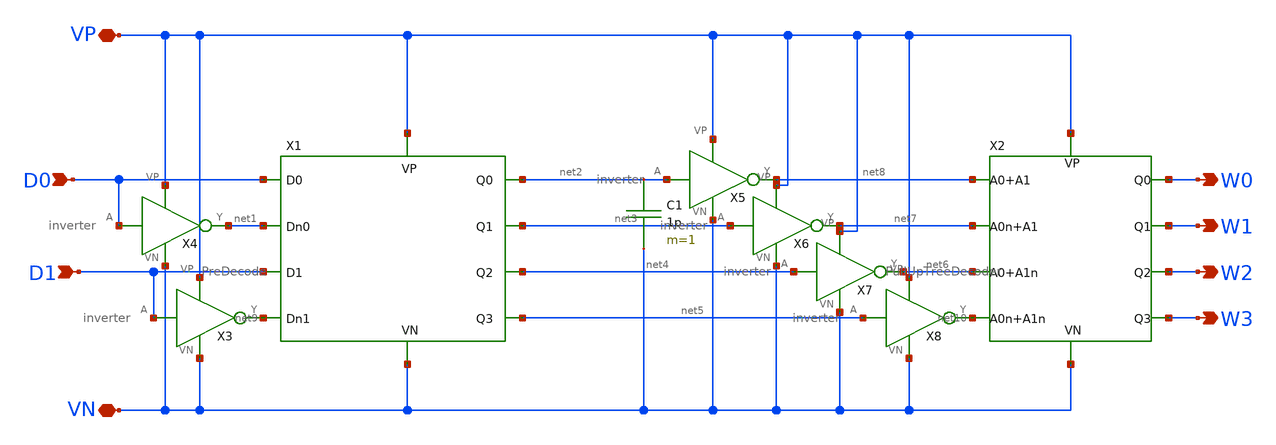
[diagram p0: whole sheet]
** sch_path: DRAM_Components/Schematic/Decoder.sch
**.subckt Decoder D1 D0 VP VN W0 W1 W2 W3
*.ipin D1
*.ipin D0
*.iopin VP
*.iopin VN
*.opin W0
*.opin W1
*.opin W2
*.opin W3
X1 net2 VP VN net3 net4 net5 net9 D1 net1 D0 PreDecode
X3 D1 net9 VP VN inverter
X4 D0 net1 VP VN inverter
X2 W0 VP VN W1 W2 W3 net10 net6 net7 net8 PullUpTreeDecoder
X5 net2 net8 VP VN inverter
X7 net4 net6 VP VN inverter
X8 net5 net10 VP VN inverter
C1 net2 VN 1p m=1
X6 net3 net7 VP VN inverter
**.ends

* expanding   symbol:  /home/madvlsi/Desktop/CMOSDRAM/DRAM_Components/Schematic/PreDecode.sym # of
*+ pins=10
** sym_path: DRAM_Components/Schematic/PreDecode.sym
** sch_path: DRAM_Components/Schematic/PreDecode.sch
.subckt PreDecode Q0 VP VN Q1 Q2 Q3 A1n A1 A0n A0
*.ipin A0
*.ipin A0n
*.ipin A1
*.ipin A1n
*.opin Q0
*.opin Q1
*.opin Q2
*.opin Q3
*.iopin VP
*.iopin VN
XM2 VP A1n net2 VP sky130_fd_pr__pfet_01v8 L=0.15 W=4 nf=1 ad='int((nf+1)/2) * W/nf * 0.29' as='int((nf+2)/2) * W/nf * 0.29'
+ pd='2*int((nf+1)/2) * (W/nf + 0.29)' ps='2*int((nf+2)/2) * (W/nf + 0.29)' nrd='0.29 / W' nrs='0.29 / W'
+ sa=0 sb=0 sd=0 mult=1 m=1
XM1 VP A1 net1 VP sky130_fd_pr__pfet_01v8 L=0.15 W=4 nf=1 ad='int((nf+1)/2) * W/nf * 0.29' as='int((nf+2)/2) * W/nf * 0.29'
+ pd='2*int((nf+1)/2) * (W/nf + 0.29)' ps='2*int((nf+2)/2) * (W/nf + 0.29)' nrd='0.29 / W' nrs='0.29 / W'
+ sa=0 sb=0 sd=0 mult=1 m=1
XM5 Q0 A0 VN VN sky130_fd_pr__nfet_01v8 L=0.15 W=1 nf=1 ad='int((nf+1)/2) * W/nf * 0.29' as='int((nf+2)/2) * W/nf * 0.29'
+ pd='2*int((nf+1)/2) * (W/nf + 0.29)' ps='2*int((nf+2)/2) * (W/nf + 0.29)' nrd='0.29 / W' nrs='0.29 / W'
+ sa=0 sb=0 sd=0 mult=1 m=1
XM3 Q1 A0n net1 VP sky130_fd_pr__pfet_01v8 L=0.15 W=2 nf=1 ad='int((nf+1)/2) * W/nf * 0.29' as='int((nf+2)/2) * W/nf * 0.29'
+ pd='2*int((nf+1)/2) * (W/nf + 0.29)' ps='2*int((nf+2)/2) * (W/nf + 0.29)' nrd='0.29 / W' nrs='0.29 / W'
+ sa=0 sb=0 sd=0 mult=1 m=1
XM4 Q0 A0 net1 VP sky130_fd_pr__pfet_01v8 L=0.15 W=2 nf=1 ad='int((nf+1)/2) * W/nf * 0.29' as='int((nf+2)/2) * W/nf * 0.29'
+ pd='2*int((nf+1)/2) * (W/nf + 0.29)' ps='2*int((nf+2)/2) * (W/nf + 0.29)' nrd='0.29 / W' nrs='0.29 / W'
+ sa=0 sb=0 sd=0 mult=1 m=1
XM6 Q0 A0 VN VN sky130_fd_pr__nfet_01v8 L=0.15 W=1 nf=1 ad='int((nf+1)/2) * W/nf * 0.29' as='int((nf+2)/2) * W/nf * 0.29'
+ pd='2*int((nf+1)/2) * (W/nf + 0.29)' ps='2*int((nf+2)/2) * (W/nf + 0.29)' nrd='0.29 / W' nrs='0.29 / W'
+ sa=0 sb=0 sd=0 mult=1 m=1
XM7 Q1 A0n VN VN sky130_fd_pr__nfet_01v8 L=0.15 W=1 nf=1 ad='int((nf+1)/2) * W/nf * 0.29' as='int((nf+2)/2) * W/nf * 0.29'
+ pd='2*int((nf+1)/2) * (W/nf + 0.29)' ps='2*int((nf+2)/2) * (W/nf + 0.29)' nrd='0.29 / W' nrs='0.29 / W'
+ sa=0 sb=0 sd=0 mult=1 m=1
XM8 Q1 A0n VN VN sky130_fd_pr__nfet_01v8 L=0.15 W=1 nf=1 ad='int((nf+1)/2) * W/nf * 0.29' as='int((nf+2)/2) * W/nf * 0.29'
+ pd='2*int((nf+1)/2) * (W/nf + 0.29)' ps='2*int((nf+2)/2) * (W/nf + 0.29)' nrd='0.29 / W' nrs='0.29 / W'
+ sa=0 sb=0 sd=0 mult=1 m=1
XM9 Q2 A1 VN VN sky130_fd_pr__nfet_01v8 L=0.15 W=1 nf=1 ad='int((nf+1)/2) * W/nf * 0.29' as='int((nf+2)/2) * W/nf * 0.29'
+ pd='2*int((nf+1)/2) * (W/nf + 0.29)' ps='2*int((nf+2)/2) * (W/nf + 0.29)' nrd='0.29 / W' nrs='0.29 / W'
+ sa=0 sb=0 sd=0 mult=1 m=1
XM10 Q2 A1 VN VN sky130_fd_pr__nfet_01v8 L=0.15 W=1 nf=1 ad='int((nf+1)/2) * W/nf * 0.29' as='int((nf+2)/2) * W/nf * 0.29'
+ pd='2*int((nf+1)/2) * (W/nf + 0.29)' ps='2*int((nf+2)/2) * (W/nf + 0.29)' nrd='0.29 / W' nrs='0.29 / W'
+ sa=0 sb=0 sd=0 mult=1 m=1
XM11 Q3 A1n VN VN sky130_fd_pr__nfet_01v8 L=0.15 W=1 nf=1 ad='int((nf+1)/2) * W/nf * 0.29' as='int((nf+2)/2) * W/nf * 0.29'
+ pd='2*int((nf+1)/2) * (W/nf + 0.29)' ps='2*int((nf+2)/2) * (W/nf + 0.29)' nrd='0.29 / W' nrs='0.29 / W'
+ sa=0 sb=0 sd=0 mult=1 m=1
XM12 Q3 A1n VN VN sky130_fd_pr__nfet_01v8 L=0.15 W=1 nf=1 ad='int((nf+1)/2) * W/nf * 0.29' as='int((nf+2)/2) * W/nf * 0.29'
+ pd='2*int((nf+1)/2) * (W/nf + 0.29)' ps='2*int((nf+2)/2) * (W/nf + 0.29)' nrd='0.29 / W' nrs='0.29 / W'
+ sa=0 sb=0 sd=0 mult=1 m=1
XM13 Q3 A1n net2 VP sky130_fd_pr__pfet_01v8 L=0.15 W=2 nf=1 ad='int((nf+1)/2) * W/nf * 0.29' as='int((nf+2)/2) * W/nf * 0.29'
+ pd='2*int((nf+1)/2) * (W/nf + 0.29)' ps='2*int((nf+2)/2) * (W/nf + 0.29)' nrd='0.29 / W' nrs='0.29 / W'
+ sa=0 sb=0 sd=0 mult=1 m=1
XM14 Q2 A1 net2 VP sky130_fd_pr__pfet_01v8 L=0.15 W=2 nf=1 ad='int((nf+1)/2) * W/nf * 0.29' as='int((nf+2)/2) * W/nf * 0.29'
+ pd='2*int((nf+1)/2) * (W/nf + 0.29)' ps='2*int((nf+2)/2) * (W/nf + 0.29)' nrd='0.29 / W' nrs='0.29 / W'
+ sa=0 sb=0 sd=0 mult=1 m=1
.ends


* expanding   symbol:  /home/madvlsi/Desktop/CMOSDRAM/DRAM_Components/Schematic/inverter.sym # of
*+ pins=4
** sym_path: DRAM_Components/Schematic/inverter.sym
** sch_path: DRAM_Components/Schematic/inverter.sch
.subckt inverter A Y VP VN
*.ipin A
*.iopin VP
*.opin Y
*.iopin VN
XM1 Y A VP VP sky130_fd_pr__pfet_01v8 L=0.15 W=1 nf=1 ad='int((nf+1)/2) * W/nf * 0.29' as='int((nf+2)/2) * W/nf * 0.29'
+ pd='2*int((nf+1)/2) * (W/nf + 0.29)' ps='2*int((nf+2)/2) * (W/nf + 0.29)' nrd='0.29 / W' nrs='0.29 / W'
+ sa=0 sb=0 sd=0 mult=1 m=1
XM2 Y A VN VN sky130_fd_pr__nfet_01v8 L=0.15 W=1 nf=1 ad='int((nf+1)/2) * W/nf * 0.29' as='int((nf+2)/2) * W/nf * 0.29'
+ pd='2*int((nf+1)/2) * (W/nf + 0.29)' ps='2*int((nf+2)/2) * (W/nf + 0.29)' nrd='0.29 / W' nrs='0.29 / W'
+ sa=0 sb=0 sd=0 mult=1 m=1
.ends


* expanding   symbol:
*+  /home/madvlsi/Desktop/CMOSDRAM/DRAM_Components/Schematic/PullUpTreeDecoder.sym # of pins=10
** sym_path: DRAM_Components/Schematic/PullUpTreeDecoder.sym
** sch_path: DRAM_Components/Schematic/PullUpTreeDecoder.sch
.subckt PullUpTreeDecoder Q0 VP VN Q1 Q2 Q3 A0nA1n A0A1n A0nA1 A0A1
*.iopin VP
*.iopin VN
*.ipin A0A1
*.ipin A0nA1
*.ipin A0A1n
*.ipin A0nA1n
*.opin Q0
*.opin Q1
*.opin Q2
*.opin Q3
XM2 Q0 A0A1 VN VN sky130_fd_pr__nfet_01v8 L=0.15 W=2 nf=1 ad='int((nf+1)/2) * W/nf * 0.29' as='int((nf+2)/2) * W/nf * 0.29'
+ pd='2*int((nf+1)/2) * (W/nf + 0.29)' ps='2*int((nf+2)/2) * (W/nf + 0.29)' nrd='0.29 / W' nrs='0.29 / W'
+ sa=0 sb=0 sd=0 mult=1 m=1
XM3 Q1 A0nA1 VP VP sky130_fd_pr__pfet_01v8 L=0.15 W=4 nf=1 ad='int((nf+1)/2) * W/nf * 0.29' as='int((nf+2)/2) * W/nf * 0.29'
+ pd='2*int((nf+1)/2) * (W/nf + 0.29)' ps='2*int((nf+2)/2) * (W/nf + 0.29)' nrd='0.29 / W' nrs='0.29 / W'
+ sa=0 sb=0 sd=0 mult=1 m=1
XM4 Q0 A0A1 VP VP sky130_fd_pr__pfet_01v8 L=0.15 W=4 nf=1 ad='int((nf+1)/2) * W/nf * 0.29' as='int((nf+2)/2) * W/nf * 0.29'
+ pd='2*int((nf+1)/2) * (W/nf + 0.29)' ps='2*int((nf+2)/2) * (W/nf + 0.29)' nrd='0.29 / W' nrs='0.29 / W'
+ sa=0 sb=0 sd=0 mult=1 m=1
XM5 Q2 A0A1n VP VP sky130_fd_pr__pfet_01v8 L=0.15 W=4 nf=1 ad='int((nf+1)/2) * W/nf * 0.29' as='int((nf+2)/2) * W/nf * 0.29'
+ pd='2*int((nf+1)/2) * (W/nf + 0.29)' ps='2*int((nf+2)/2) * (W/nf + 0.29)' nrd='0.29 / W' nrs='0.29 / W'
+ sa=0 sb=0 sd=0 mult=1 m=1
XM6 Q3 A0nA1n VP VP sky130_fd_pr__pfet_01v8 L=0.15 W=4 nf=1 ad='int((nf+1)/2) * W/nf * 0.29' as='int((nf+2)/2) * W/nf * 0.29'
+ pd='2*int((nf+1)/2) * (W/nf + 0.29)' ps='2*int((nf+2)/2) * (W/nf + 0.29)' nrd='0.29 / W' nrs='0.29 / W'
+ sa=0 sb=0 sd=0 mult=1 m=1
XM7 Q1 A0nA1 VN VN sky130_fd_pr__nfet_01v8 L=0.15 W=2 nf=1 ad='int((nf+1)/2) * W/nf * 0.29' as='int((nf+2)/2) * W/nf * 0.29'
+ pd='2*int((nf+1)/2) * (W/nf + 0.29)' ps='2*int((nf+2)/2) * (W/nf + 0.29)' nrd='0.29 / W' nrs='0.29 / W'
+ sa=0 sb=0 sd=0 mult=1 m=1
XM8 Q2 A0A1n VN VN sky130_fd_pr__nfet_01v8 L=0.15 W=2 nf=1 ad='int((nf+1)/2) * W/nf * 0.29' as='int((nf+2)/2) * W/nf * 0.29'
+ pd='2*int((nf+1)/2) * (W/nf + 0.29)' ps='2*int((nf+2)/2) * (W/nf + 0.29)' nrd='0.29 / W' nrs='0.29 / W'
+ sa=0 sb=0 sd=0 mult=1 m=1
XM9 Q3 A0nA1n VN VN sky130_fd_pr__nfet_01v8 L=0.15 W=2 nf=1 ad='int((nf+1)/2) * W/nf * 0.29' as='int((nf+2)/2) * W/nf * 0.29'
+ pd='2*int((nf+1)/2) * (W/nf + 0.29)' ps='2*int((nf+2)/2) * (W/nf + 0.29)' nrd='0.29 / W' nrs='0.29 / W'
+ sa=0 sb=0 sd=0 mult=1 m=1
XM1 VP VP Q0 VP sky130_fd_pr__pfet_01v8 L=0.15 W=4 nf=1 ad='int((nf+1)/2) * W/nf * 0.29' as='int((nf+2)/2) * W/nf * 0.29'
+ pd='2*int((nf+1)/2) * (W/nf + 0.29)' ps='2*int((nf+2)/2) * (W/nf + 0.29)' nrd='0.29 / W' nrs='0.29 / W'
+ sa=0 sb=0 sd=0 mult=1 m=1
XM10 VN VN Q0 VN sky130_fd_pr__nfet_01v8 L=0.15 W=2 nf=1 ad='int((nf+1)/2) * W/nf * 0.29' as='int((nf+2)/2) * W/nf * 0.29'
+ pd='2*int((nf+1)/2) * (W/nf + 0.29)' ps='2*int((nf+2)/2) * (W/nf + 0.29)' nrd='0.29 / W' nrs='0.29 / W'
+ sa=0 sb=0 sd=0 mult=1 m=1
XM11 VN VN Q3 VN sky130_fd_pr__nfet_01v8 L=0.15 W=2 nf=1 ad='int((nf+1)/2) * W/nf * 0.29' as='int((nf+2)/2) * W/nf * 0.29'
+ pd='2*int((nf+1)/2) * (W/nf + 0.29)' ps='2*int((nf+2)/2) * (W/nf + 0.29)' nrd='0.29 / W' nrs='0.29 / W'
+ sa=0 sb=0 sd=0 mult=1 m=1
XM12 VN VN Q1 VN sky130_fd_pr__nfet_01v8 L=0.15 W=2 nf=1 ad='int((nf+1)/2) * W/nf * 0.29' as='int((nf+2)/2) * W/nf * 0.29'
+ pd='2*int((nf+1)/2) * (W/nf + 0.29)' ps='2*int((nf+2)/2) * (W/nf + 0.29)' nrd='0.29 / W' nrs='0.29 / W'
+ sa=0 sb=0 sd=0 mult=1 m=1
XM13 VN VN Q2 VN sky130_fd_pr__nfet_01v8 L=0.15 W=2 nf=1 ad='int((nf+1)/2) * W/nf * 0.29' as='int((nf+2)/2) * W/nf * 0.29'
+ pd='2*int((nf+1)/2) * (W/nf + 0.29)' ps='2*int((nf+2)/2) * (W/nf + 0.29)' nrd='0.29 / W' nrs='0.29 / W'
+ sa=0 sb=0 sd=0 mult=1 m=1
XM14 VP VP Q1 VP sky130_fd_pr__pfet_01v8 L=0.15 W=4 nf=1 ad='int((nf+1)/2) * W/nf * 0.29' as='int((nf+2)/2) * W/nf * 0.29'
+ pd='2*int((nf+1)/2) * (W/nf + 0.29)' ps='2*int((nf+2)/2) * (W/nf + 0.29)' nrd='0.29 / W' nrs='0.29 / W'
+ sa=0 sb=0 sd=0 mult=1 m=1
XM15 Q2 VP VP VP sky130_fd_pr__pfet_01v8 L=0.15 W=4 nf=1 ad='int((nf+1)/2) * W/nf * 0.29' as='int((nf+2)/2) * W/nf * 0.29'
+ pd='2*int((nf+1)/2) * (W/nf + 0.29)' ps='2*int((nf+2)/2) * (W/nf + 0.29)' nrd='0.29 / W' nrs='0.29 / W'
+ sa=0 sb=0 sd=0 mult=1 m=1
XM16 VP VP Q3 VP sky130_fd_pr__pfet_01v8 L=0.15 W=4 nf=1 ad='int((nf+1)/2) * W/nf * 0.29' as='int((nf+2)/2) * W/nf * 0.29'
+ pd='2*int((nf+1)/2) * (W/nf + 0.29)' ps='2*int((nf+2)/2) * (W/nf + 0.29)' nrd='0.29 / W' nrs='0.29 / W'
+ sa=0 sb=0 sd=0 mult=1 m=1
.ends

.end
